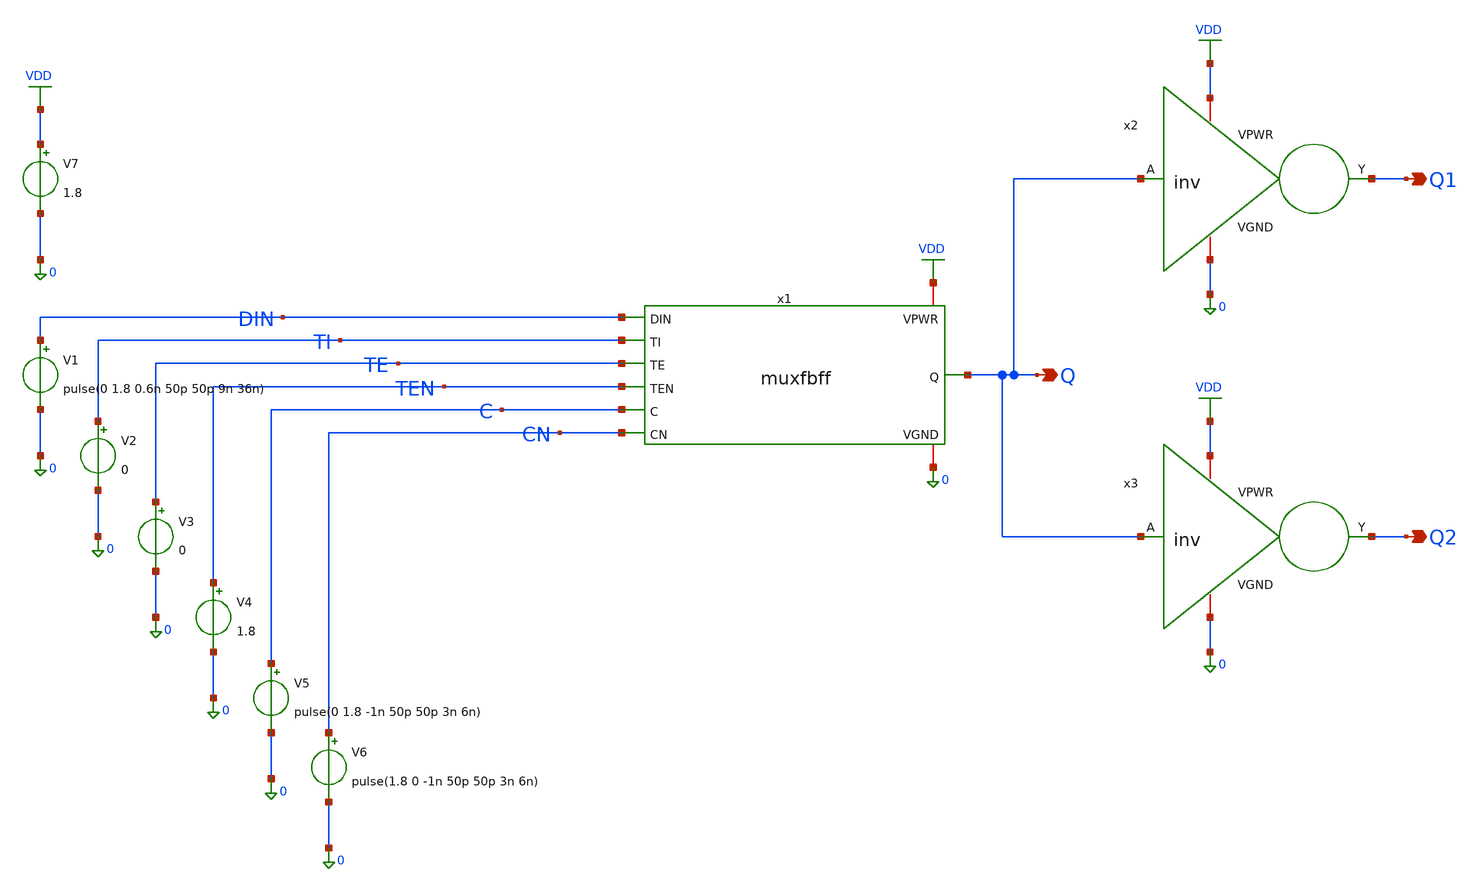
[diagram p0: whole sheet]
** sch_path: muxfbff/dataModefall/muxfbff_tb_datamode_fall.sch
**.subckt muxfbff_tb_datamode_fall Q Q1 Q2
*.opin Q
*.opin Q1
*.opin Q2
V1 DIN 0 pulse(0 1.8 0.6n 50p 50p 9n 36n)
V2 TI 0 0
V3 TE 0 0
V4 TEN 0 1.8
V5 C 0 pulse(0 1.8 -1n 50p 50p 3n 6n)
V6 CN 0 pulse(1.8 0 -1n 50p 50p 3n 6n)
V7 VDD 0 1.8
x2 VDD Q Q1 0 inv
x3 VDD Q Q2 0 inv
x1 VDD 0 Q DIN TI TE TEN C CN muxfbff
**** begin user architecture code

** opencircuitdesign pdks install
.lib $::SKYWATER_MODELS/sky130.lib.spice tt




.tran 0.001n 20n
.control
  save all
  shell rm -f /home/sushanth/Desktop/HighSpeedScanFlop/muxfbff/dataModefall/outputsim.txt

    run
	meas tran cq_delay TRIG v(C) VAL=0.9 RISE=2 TARG v(Q) VAL=0.9 FALL=1
	meas tran dc_delay TRIG v(din) VAL=0.9 FALL=1 TARG v(C) VAL=0.9 RISE=2
	print v(c),v(din),v(q) >
+ /home/sushanth/Desktop/HighSpeedScanFlop/muxfbff/dataModefall/outputsim.txt
  end
.endc





**** end user architecture code
**.ends
.GLOBAL VDD
.end
